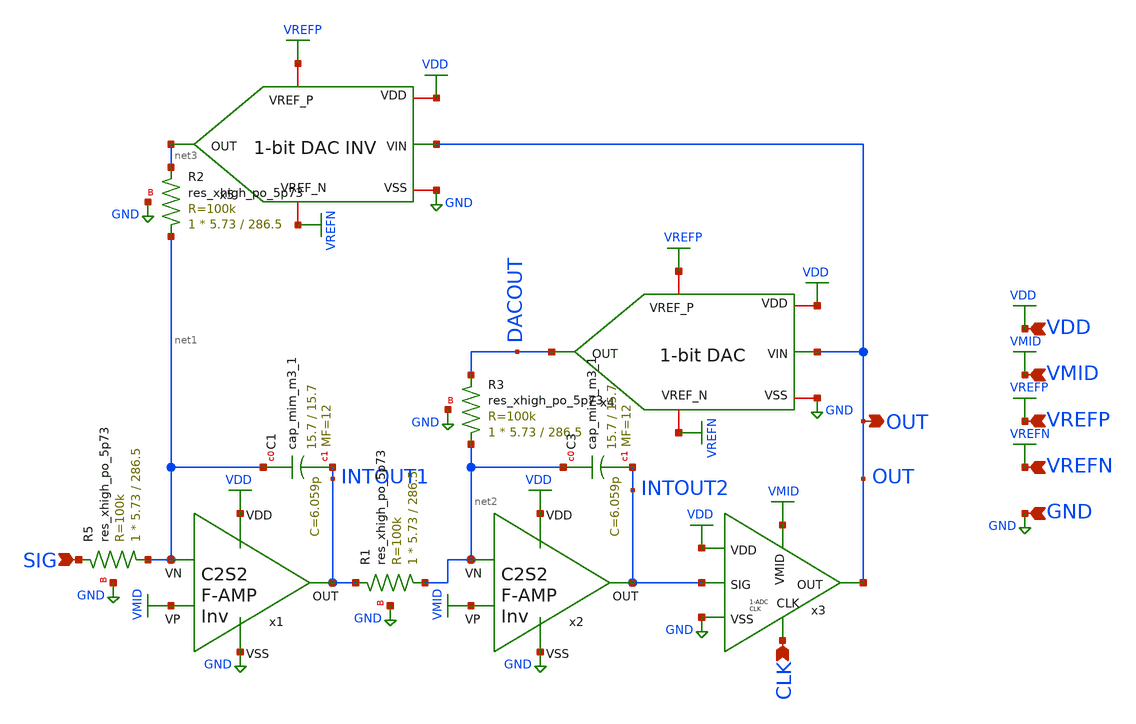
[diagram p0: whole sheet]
** sch_path: SP24_caravel_user_project_analog/xschem/xschem_DeltaSigma/DS_2024_3p0.sch
.lib $::SKYWATER_MODELS/sky130.lib.spice tt
.include $::SKYWATER_STDCELLS/sky130_fd_sc_hd.spice

**.subckt DS_2024_3p0 SIG CLK VDD VMID VREFP OUT VREFN GND
*.ipin SIG
*.ipin CLK
*.ipin VDD
*.ipin VMID
*.ipin VREFP
*.opin OUT
*.ipin VREFN
*.ipin GND
x1 VDD VMID net1 INTOUT1 GND C2S2_Amp_F_I
x2 VDD VMID net2 INTOUT2 GND C2S2_Amp_F_I
x5 VREFP VDD net3 OUT GND VREFN 1Bit_DAC_Inv
x4 VREFP VDD DACOUT OUT GND VREFN 1Bit_DAC
x3 VDD INTOUT2 OUT CLK GND VMID 1Bit_Clk_ADC
XR5 net1 SIG GND sky130_fd_pr__res_xhigh_po_5p73 L=286.5 mult=1 m=1
XR1 net2 INTOUT1 GND sky130_fd_pr__res_xhigh_po_5p73 L=286.5 mult=1 m=1
XR2 net1 net3 GND sky130_fd_pr__res_xhigh_po_5p73 L=286.5 mult=1 m=1
XR3 net2 DACOUT GND sky130_fd_pr__res_xhigh_po_5p73 L=286.5 mult=1 m=1
XC3 net2 INTOUT2 sky130_fd_pr__cap_mim_m3_1 W=15.7 L=15.7 MF=12 m=12
XC1 net1 INTOUT1 sky130_fd_pr__cap_mim_m3_1 W=15.7 L=15.7 MF=12 m=12
**.ends
.GLOBAL VDD
.GLOBAL GND
.GLOBAL VMID
.GLOBAL VREFP
.GLOBAL VREFN
.end
